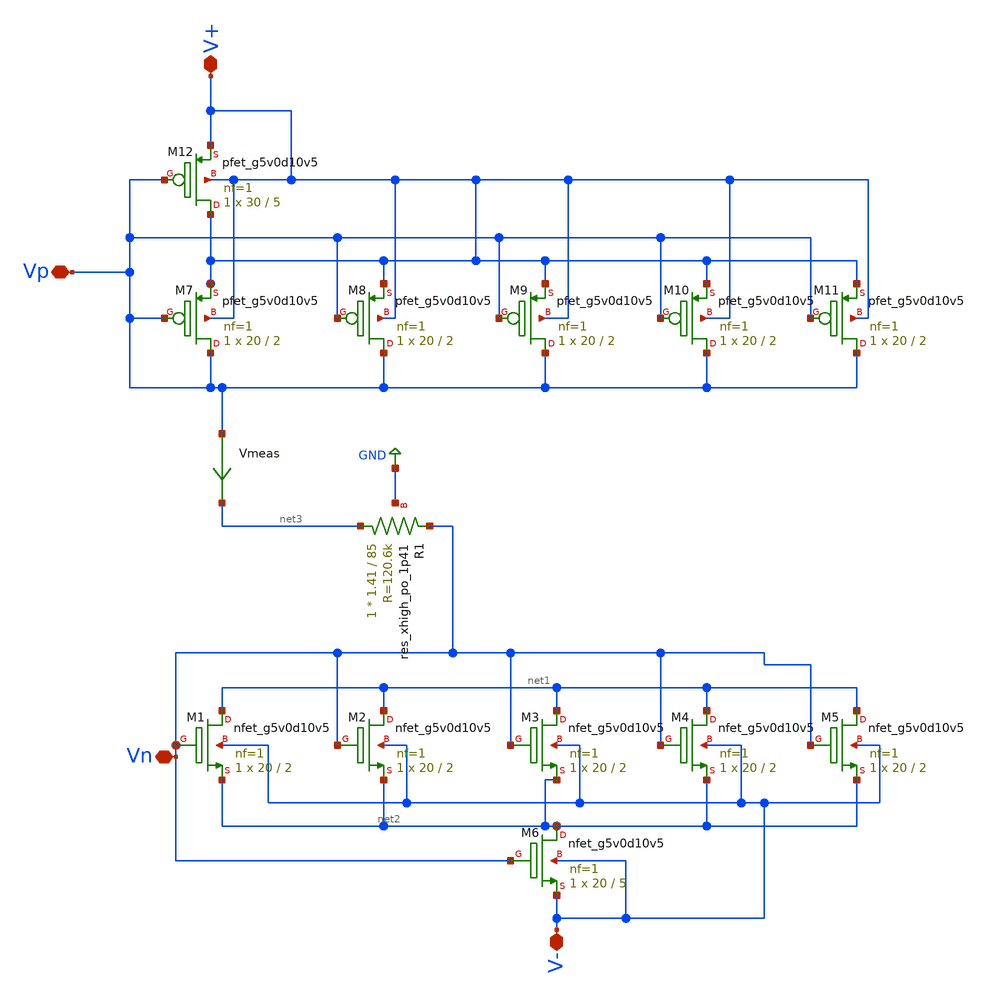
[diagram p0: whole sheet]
** sch_path: xschem/PrimalStructures/CurRef1.sch
**.subckt CurRef1 Vp V+ V- Vn
*.iopin Vp
*.iopin V+
*.iopin V-
*.iopin Vn
XM1 net1 Vn net2 V- sky130_fd_pr__nfet_g5v0d10v5 L=2 W=20 nf=1 ad='int((nf+1)/2) * W/nf * 0.29' as='int((nf+2)/2) * W/nf * 0.29'
+ pd='2*int((nf+1)/2) * (W/nf + 0.29)' ps='2*int((nf+2)/2) * (W/nf + 0.29)' nrd='0.29 / W' nrs='0.29 / W'
+ sa=0 sb=0 sd=0 mult=1 m=1
XM2 net1 Vn net2 V- sky130_fd_pr__nfet_g5v0d10v5 L=2 W=20 nf=1 ad='int((nf+1)/2) * W/nf * 0.29' as='int((nf+2)/2) * W/nf * 0.29'
+ pd='2*int((nf+1)/2) * (W/nf + 0.29)' ps='2*int((nf+2)/2) * (W/nf + 0.29)' nrd='0.29 / W' nrs='0.29 / W'
+ sa=0 sb=0 sd=0 mult=1 m=1
XM3 net1 Vn net2 V- sky130_fd_pr__nfet_g5v0d10v5 L=2 W=20 nf=1 ad='int((nf+1)/2) * W/nf * 0.29' as='int((nf+2)/2) * W/nf * 0.29'
+ pd='2*int((nf+1)/2) * (W/nf + 0.29)' ps='2*int((nf+2)/2) * (W/nf + 0.29)' nrd='0.29 / W' nrs='0.29 / W'
+ sa=0 sb=0 sd=0 mult=1 m=1
XM4 net1 Vn net2 V- sky130_fd_pr__nfet_g5v0d10v5 L=2 W=20 nf=1 ad='int((nf+1)/2) * W/nf * 0.29' as='int((nf+2)/2) * W/nf * 0.29'
+ pd='2*int((nf+1)/2) * (W/nf + 0.29)' ps='2*int((nf+2)/2) * (W/nf + 0.29)' nrd='0.29 / W' nrs='0.29 / W'
+ sa=0 sb=0 sd=0 mult=1 m=1
XM5 net1 Vn net2 V- sky130_fd_pr__nfet_g5v0d10v5 L=2 W=20 nf=1 ad='int((nf+1)/2) * W/nf * 0.29' as='int((nf+2)/2) * W/nf * 0.29'
+ pd='2*int((nf+1)/2) * (W/nf + 0.29)' ps='2*int((nf+2)/2) * (W/nf + 0.29)' nrd='0.29 / W' nrs='0.29 / W'
+ sa=0 sb=0 sd=0 mult=1 m=1
XM6 net2 Vn V- V- sky130_fd_pr__nfet_g5v0d10v5 L=5 W=20 nf=1 ad='int((nf+1)/2) * W/nf * 0.29' as='int((nf+2)/2) * W/nf * 0.29'
+ pd='2*int((nf+1)/2) * (W/nf + 0.29)' ps='2*int((nf+2)/2) * (W/nf + 0.29)' nrd='0.29 / W' nrs='0.29 / W'
+ sa=0 sb=0 sd=0 mult=1 m=1
XR1 net3 Vn GND sky130_fd_pr__res_xhigh_po_1p41 L=85 mult=1 m=1
XM7 Vp Vp V+ V+ sky130_fd_pr__pfet_g5v0d10v5 L=2 W=20 nf=1 ad='int((nf+1)/2) * W/nf * 0.29' as='int((nf+2)/2) * W/nf * 0.29'
+ pd='2*int((nf+1)/2) * (W/nf + 0.29)' ps='2*int((nf+2)/2) * (W/nf + 0.29)' nrd='0.29 / W' nrs='0.29 / W'
+ sa=0 sb=0 sd=0 mult=1 m=1
XM8 Vp Vp V+ V+ sky130_fd_pr__pfet_g5v0d10v5 L=2 W=20 nf=1 ad='int((nf+1)/2) * W/nf * 0.29' as='int((nf+2)/2) * W/nf * 0.29'
+ pd='2*int((nf+1)/2) * (W/nf + 0.29)' ps='2*int((nf+2)/2) * (W/nf + 0.29)' nrd='0.29 / W' nrs='0.29 / W'
+ sa=0 sb=0 sd=0 mult=1 m=1
XM9 Vp Vp V+ V+ sky130_fd_pr__pfet_g5v0d10v5 L=2 W=20 nf=1 ad='int((nf+1)/2) * W/nf * 0.29' as='int((nf+2)/2) * W/nf * 0.29'
+ pd='2*int((nf+1)/2) * (W/nf + 0.29)' ps='2*int((nf+2)/2) * (W/nf + 0.29)' nrd='0.29 / W' nrs='0.29 / W'
+ sa=0 sb=0 sd=0 mult=1 m=1
XM10 Vp Vp V+ V+ sky130_fd_pr__pfet_g5v0d10v5 L=2 W=20 nf=1 ad='int((nf+1)/2) * W/nf * 0.29' as='int((nf+2)/2) * W/nf * 0.29'
+ pd='2*int((nf+1)/2) * (W/nf + 0.29)' ps='2*int((nf+2)/2) * (W/nf + 0.29)' nrd='0.29 / W' nrs='0.29 / W'
+ sa=0 sb=0 sd=0 mult=1 m=1
XM11 Vp Vp V+ V+ sky130_fd_pr__pfet_g5v0d10v5 L=2 W=20 nf=1 ad='int((nf+1)/2) * W/nf * 0.29' as='int((nf+2)/2) * W/nf * 0.29'
+ pd='2*int((nf+1)/2) * (W/nf + 0.29)' ps='2*int((nf+2)/2) * (W/nf + 0.29)' nrd='0.29 / W' nrs='0.29 / W'
+ sa=0 sb=0 sd=0 mult=1 m=1
XM12 V+ Vp V+ V+ sky130_fd_pr__pfet_g5v0d10v5 L=5 W=30 nf=1 ad='int((nf+1)/2) * W/nf * 0.29' as='int((nf+2)/2) * W/nf * 0.29'
+ pd='2*int((nf+1)/2) * (W/nf + 0.29)' ps='2*int((nf+2)/2) * (W/nf + 0.29)' nrd='0.29 / W' nrs='0.29 / W'
+ sa=0 sb=0 sd=0 mult=1 m=1
Vmeas Vp net3 0
.save i(vmeas)
**** begin user architecture code

** opencircuitdesign pdks install
.lib $::SKYWATER_MODELS/sky130.lib.spice tt



* this option enables mos model bin
* selection based on W/NF instead of W
.control
op
print all
save all
plot I(Vmeas) vs V(Vt)

.endc


**** end user architecture code
**.ends
.GLOBAL GND
.end
